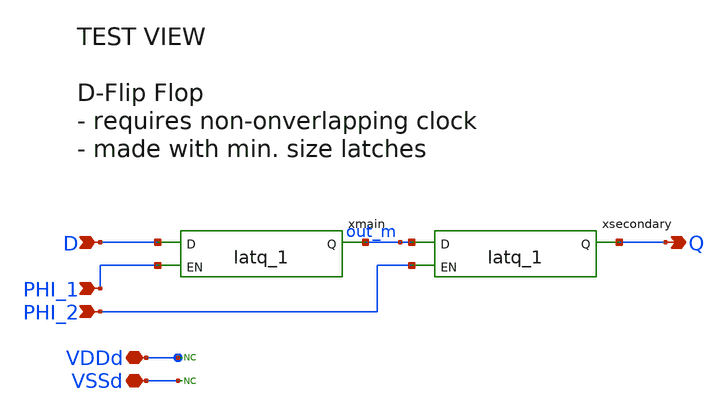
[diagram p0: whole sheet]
** sch_path: DFF_2phase_1/views/DFF_2phase_1_test.sch
**.subckt DFF_2phase_1_test D PHI_1 PHI_2 Q VDDd VSSd
*.ipin D
*.ipin PHI_1
*.ipin PHI_2
*.opin Q
*.iopin VDDd
*.iopin VSSd
xmain D PHI_1 out_m VDDd VDDd VSSd VSSd gf180mcu_fd_sc_mcu9t5v0__latq_1
xsecondary out_m PHI_2 Q VDDd VDDd VSSd VSSd gf180mcu_fd_sc_mcu9t5v0__latq_1
* noconn VSSd
* noconn VDDd
**.ends
.end
